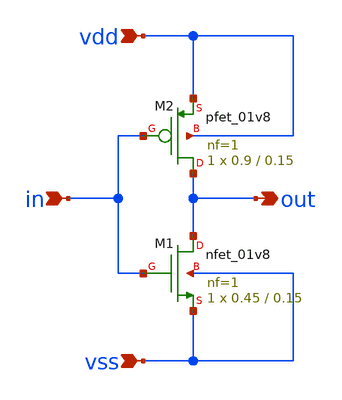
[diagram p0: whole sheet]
** sch_path: track_vlsi/ledesma/sch/inverter.sch
**.subckt inverter out in vdd vss
*.opin out
*.ipin in
*.ipin vdd
*.ipin vss
XM1 out in vss vss sky130_fd_pr__nfet_01v8 L=0.15 W=0.45 nf=1 ad='int((nf+1)/2) * W/nf * 0.29' as='int((nf+2)/2) * W/nf * 0.29'
+ pd='2*int((nf+1)/2) * (W/nf + 0.29)' ps='2*int((nf+2)/2) * (W/nf + 0.29)' nrd='0.29 / W' nrs='0.29 / W'
+ sa=0 sb=0 sd=0 mult=1 m=1
XM2 out in vdd vdd sky130_fd_pr__pfet_01v8 L=0.15 W=0.9 nf=1 ad='int((nf+1)/2) * W/nf * 0.29' as='int((nf+2)/2) * W/nf * 0.29'
+ pd='2*int((nf+1)/2) * (W/nf + 0.29)' ps='2*int((nf+2)/2) * (W/nf + 0.29)' nrd='0.29 / W' nrs='0.29 / W'
+ sa=0 sb=0 sd=0 mult=1 m=1
**.ends
.end
